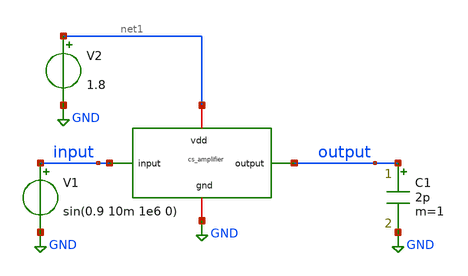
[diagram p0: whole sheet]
** sch_path: xschem/cs_amplifier_tb.sch
**.subckt cs_amplifier_tb
x1 net1 output input GND cs_amplifier
V1 input GND sin(0.9 10m 1e6 0)
V2 net1 GND 1.8
C1 output GND 2p m=1
**** begin user architecture code

** opencircuitdesign pdks install
.lib $::SKYWATER_MODELS/sky130.lib.spice tt




.control
 save all
 tran 0.01u 10u
 write cs_amplifier_tb.raw
 plot v(input) v(output)
.endc


**** end user architecture code
**.ends

* expanding   symbol:  cs_amplifier.sym # of pins=4
** sym_path: xschem/cs_amplifier.sym
** sch_path: xschem/cs_amplifier.sch
.subckt cs_amplifier vdd output input gnd
*.ipin input
*.iopin vdd
*.iopin gnd
*.opin output
XM1 output input gnd gnd sky130_fd_pr__nfet_01v8 L=0.30 W=50 nf=10 ad='int((nf+1)/2) * W/nf * 0.29' as='int((nf+2)/2) * W/nf * 0.29'
+ pd='2*int((nf+1)/2) * (W/nf + 0.29)' ps='2*int((nf+2)/2) * (W/nf + 0.29)' nrd='0.29 / W' nrs='0.29 / W'
+ sa=0 sb=0 sd=0 mult=1 m=1
XR1 output vdd gnd sky130_fd_pr__res_xhigh_po_0p35 L=0.175 mult=1 m=1
.ends

.GLOBAL GND
.end
